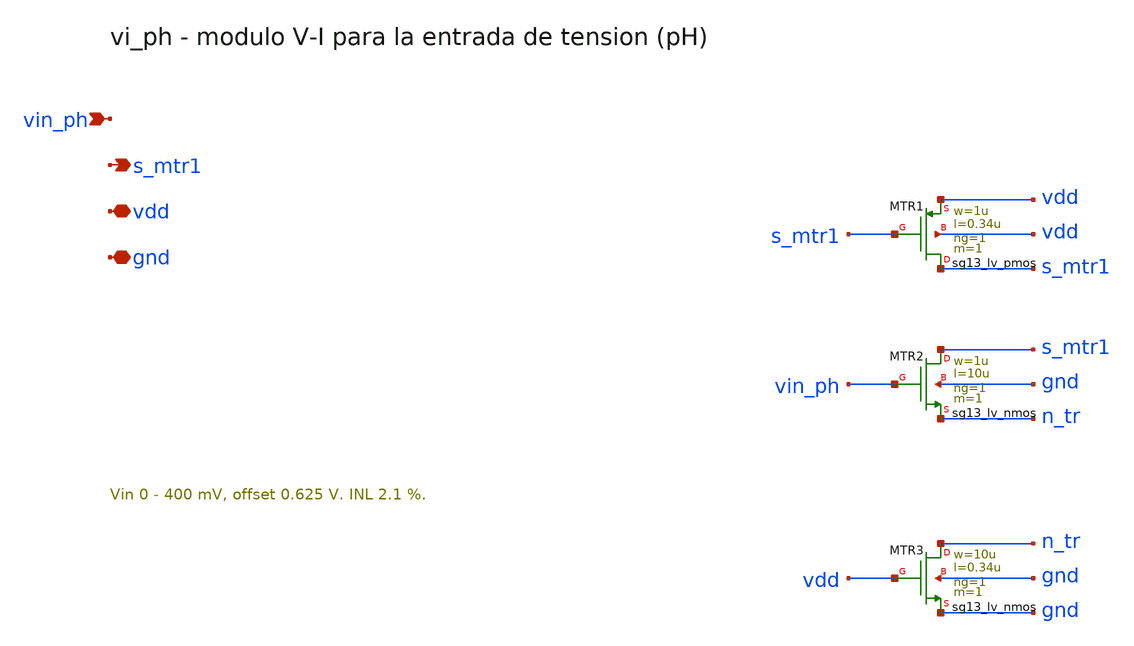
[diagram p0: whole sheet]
** sch_path: Enfoque_B/xschem/celdas/vi_ph.sch
**.subckt vi_ph vin_ph s_mtr1 vdd gnd
*.ipin vin_ph
*.opin s_mtr1
*.iopin vdd
*.iopin gnd
XMTR1 s_mtr1 s_mtr1 vdd vdd sg13_lv_pmos w=1u l=0.34u ng=1 m=1 mm_ok=1
XMTR2 s_mtr1 vin_ph n_tr gnd sg13_lv_nmos w=1u l=10u ng=1 m=1 mm_ok=1
XMTR3 n_tr vdd gnd gnd sg13_lv_nmos w=10u l=0.34u ng=1 m=1 mm_ok=1
**.ends
.end
